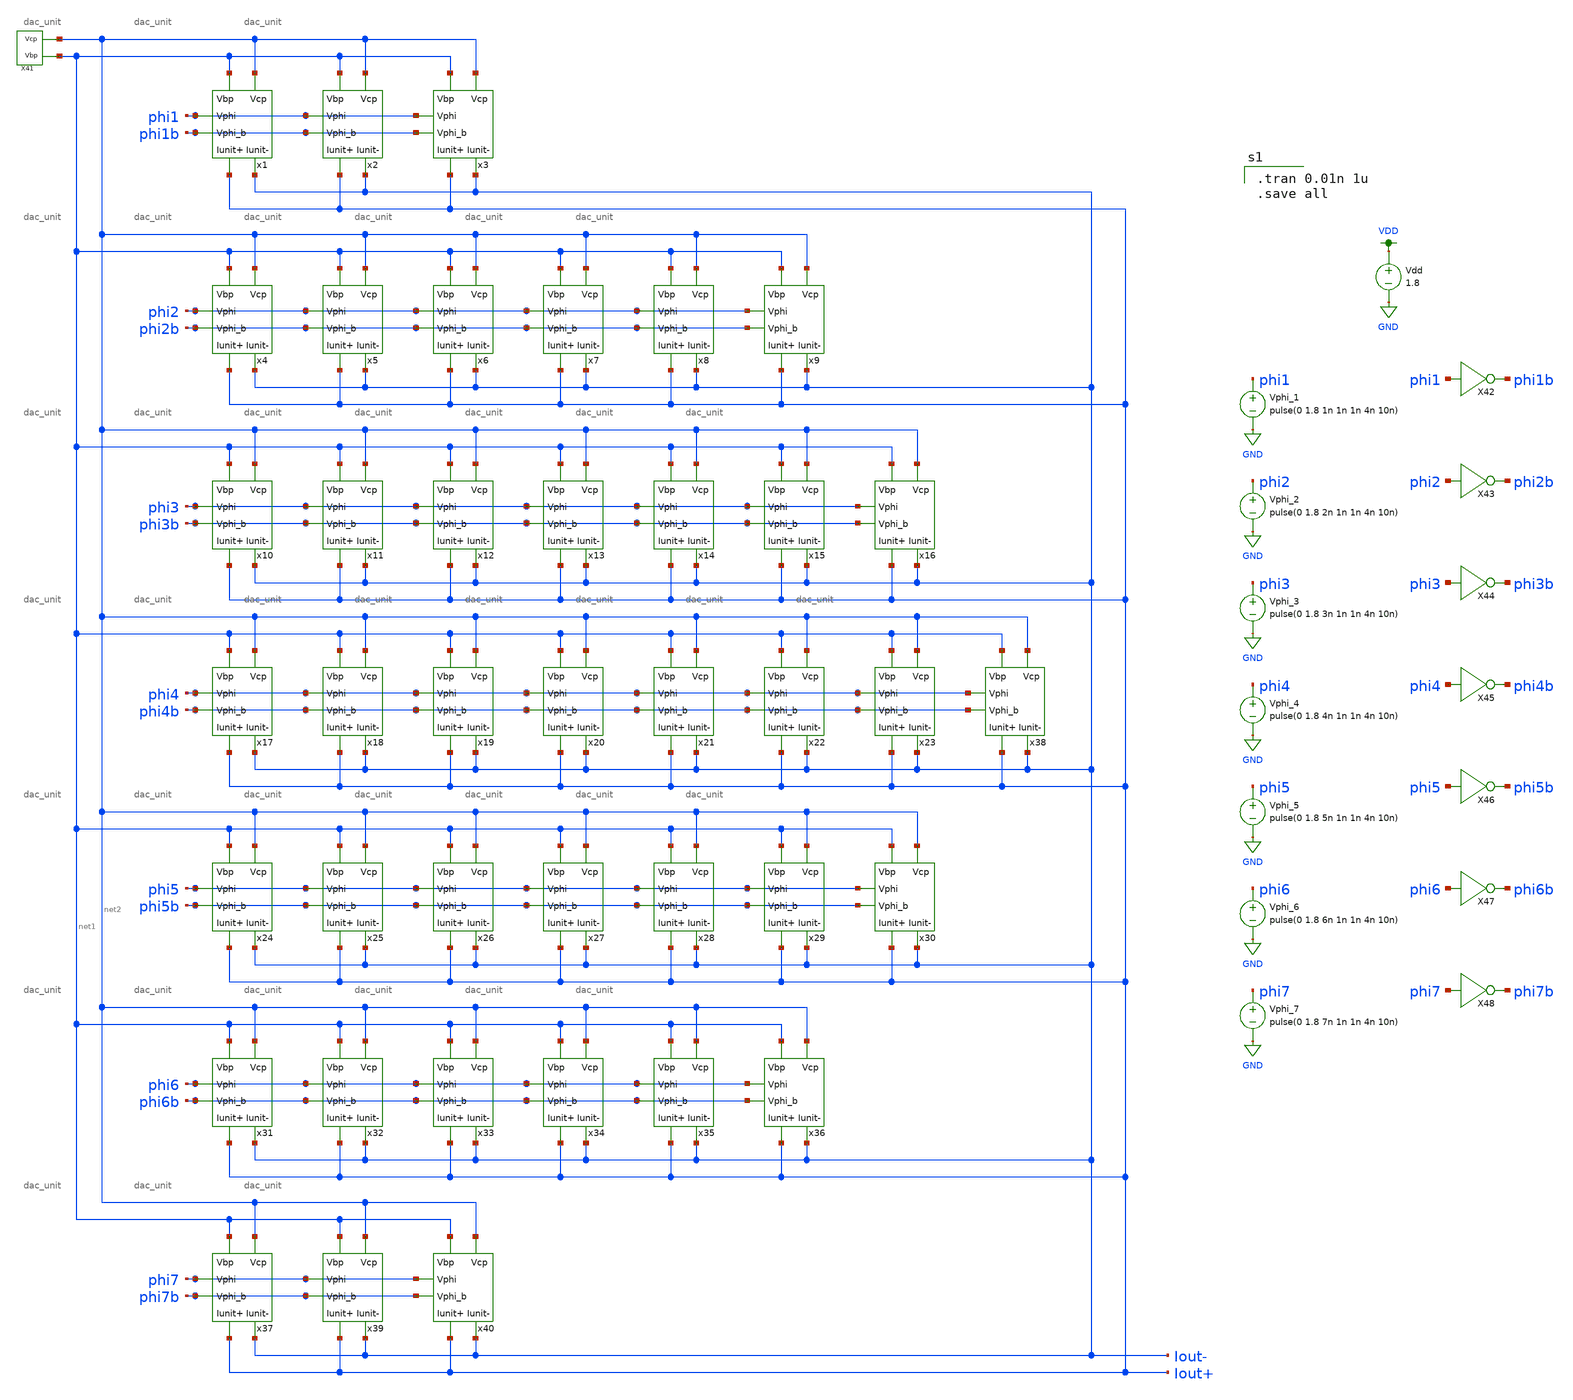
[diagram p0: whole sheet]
** sch_path: simulation/dac/dac.sch
**.subckt dac
x1 net1 net2 Iout+ Iout- phi1 phi1b dac_unit
x2 net1 net2 Iout+ Iout- phi1 phi1b dac_unit
x3 net1 net2 Iout+ Iout- phi1 phi1b dac_unit
x4 net1 net2 Iout+ Iout- phi2 phi2b dac_unit
x5 net1 net2 Iout+ Iout- phi2 phi2b dac_unit
x6 net1 net2 Iout+ Iout- phi2 phi2b dac_unit
x7 net1 net2 Iout+ Iout- phi2 phi2b dac_unit
x8 net1 net2 Iout+ Iout- phi2 phi2b dac_unit
x9 net1 net2 Iout+ Iout- phi2 phi2b dac_unit
x10 net1 net2 Iout+ Iout- phi3 phi3b dac_unit
x11 net1 net2 Iout+ Iout- phi3 phi3b dac_unit
x12 net1 net2 Iout+ Iout- phi3 phi3b dac_unit
x13 net1 net2 Iout+ Iout- phi3 phi3b dac_unit
x14 net1 net2 Iout+ Iout- phi3 phi3b dac_unit
x15 net1 net2 Iout+ Iout- phi3 phi3b dac_unit
x16 net1 net2 Iout+ Iout- phi3 phi3b dac_unit
x17 net1 net2 Iout+ Iout- phi4 phi4b dac_unit
x18 net1 net2 Iout+ Iout- phi4 phi4b dac_unit
x19 net1 net2 Iout+ Iout- phi4 phi4b dac_unit
x20 net1 net2 Iout+ Iout- phi4 phi4b dac_unit
x21 net1 net2 Iout+ Iout- phi4 phi4b dac_unit
x22 net1 net2 Iout+ Iout- phi4 phi4b dac_unit
x23 net1 net2 Iout+ Iout- phi4 phi4b dac_unit
x24 net1 net2 Iout+ Iout- phi5 phi5b dac_unit
x25 net1 net2 Iout+ Iout- phi5 phi5b dac_unit
x26 net1 net2 Iout+ Iout- phi5 phi5b dac_unit
x27 net1 net2 Iout+ Iout- phi5 phi5b dac_unit
x28 net1 net2 Iout+ Iout- phi5 phi5b dac_unit
x29 net1 net2 Iout+ Iout- phi5 phi5b dac_unit
x30 net1 net2 Iout+ Iout- phi5 phi5b dac_unit
x31 net1 net2 Iout+ Iout- phi6 phi6b dac_unit
x32 net1 net2 Iout+ Iout- phi6 phi6b dac_unit
x33 net1 net2 Iout+ Iout- phi6 phi6b dac_unit
x34 net1 net2 Iout+ Iout- phi6 phi6b dac_unit
x35 net1 net2 Iout+ Iout- phi6 phi6b dac_unit
x36 net1 net2 Iout+ Iout- phi6 phi6b dac_unit
x38 net1 net2 Iout+ Iout- phi4 phi4b dac_unit
x37 net1 net2 Iout+ Iout- phi7 phi7b dac_unit
x39 net1 net2 Iout+ Iout- phi7 phi7b dac_unit
x40 net1 net2 Iout+ Iout- phi7 phi7b dac_unit
X41 net2 net1 v_gen_lds
Vdd VDD GND 1.8
Vphi_1 phi1 GND pulse(0 1.8 1n 1n 1n 4n 10n)
Vphi_2 phi2 GND pulse(0 1.8 2n 1n 1n 4n 10n)
Vphi_3 phi3 GND pulse(0 1.8 3n 1n 1n 4n 10n)
Vphi_4 phi4 GND pulse(0 1.8 4n 1n 1n 4n 10n)
Vphi_5 phi5 GND pulse(0 1.8 5n 1n 1n 4n 10n)
Vphi_6 phi6 GND pulse(0 1.8 6n 1n 1n 4n 10n)
Vphi_7 phi7 GND pulse(0 1.8 7n 1n 1n 4n 10n)
X42 phi1 phi1b inverter
X43 phi2 phi2b inverter
X44 phi3 phi3b inverter
X45 phi4 phi4b inverter
X46 phi5 phi5b inverter
X47 phi6 phi6b inverter
X48 phi7 phi7b inverter
**** begin user architecture code

.option wnflag=1
.lib ~/skywater/skywater-pdk/libraries/sky130_fd_pr_ngspice/latest/models/sky130.lib.spice tt


.tran 0.01n 1u
.save all

**** end user architecture code
**.ends

* expanding   symbol:  ./dac_unit.sym # of pins=6
** sym_path: simulation/dac/dac_unit.sym
** sch_path: simulation/dac/dac_unit.sch
.subckt dac_unit Vbp Vcp Iunit+ Iunit- Vphi Vphi_b
*.ipin Vphi
*.ipin Vbp
*.ipin Vcp
*.opin Iunit-
*.opin Iunit+
*.ipin Vphi_b
XM1 net1 Vbp VDD VDD sky130_fd_pr__pfet_01v8 L=0.5 W=12 nf=1 ad='int((nf+1)/2) * W/nf * 0.29' as='int((nf+2)/2) * W/nf * 0.29'
+ pd='2*int((nf+1)/2) * (W/nf + 0.29)' ps='2*int((nf+2)/2) * (W/nf + 0.29)' nrd='0.29 / W' nrs='0.29 / W'
+ sa=0 sb=0 sd=0 mult=1 m=1
XM2 net2 Vcp net1 VDD sky130_fd_pr__pfet_01v8 L=0.5 W=12 nf=1 ad='int((nf+1)/2) * W/nf * 0.29' as='int((nf+2)/2) * W/nf * 0.29'
+ pd='2*int((nf+1)/2) * (W/nf + 0.29)' ps='2*int((nf+2)/2) * (W/nf + 0.29)' nrd='0.29 / W' nrs='0.29 / W'
+ sa=0 sb=0 sd=0 mult=1 m=1
XM3 Iunit- Vphi net2 VDD sky130_fd_pr__pfet_01v8 L=0.5 W=12 nf=1 ad='int((nf+1)/2) * W/nf * 0.29' as='int((nf+2)/2) * W/nf * 0.29'
+ pd='2*int((nf+1)/2) * (W/nf + 0.29)' ps='2*int((nf+2)/2) * (W/nf + 0.29)' nrd='0.29 / W' nrs='0.29 / W'
+ sa=0 sb=0 sd=0 mult=1 m=1
XM4 Iunit+ Vphi_b net2 VDD sky130_fd_pr__pfet_01v8 L=0.5 W=12 nf=1 ad='int((nf+1)/2) * W/nf * 0.29' as='int((nf+2)/2) * W/nf * 0.29'
+ pd='2*int((nf+1)/2) * (W/nf + 0.29)' ps='2*int((nf+2)/2) * (W/nf + 0.29)' nrd='0.29 / W' nrs='0.29 / W'
+ sa=0 sb=0 sd=0 mult=1 m=1
.ends


* expanding   symbol:  ./v_gen_lds.sym # of pins=2
** sym_path: simulation/dac/v_gen_lds.sym
** sch_path: simulation/dac/v_gen_lds.sch
.subckt v_gen_lds Vcp Vbp
*.opin Vcp
*.opin Vbp
XM25 net1 Vcp Vcp VDD sky130_fd_pr__pfet_01v8 L=0.5 W=12 nf=1 ad='int((nf+1)/2) * W/nf * 0.29' as='int((nf+2)/2) * W/nf * 0.29'
+ pd='2*int((nf+1)/2) * (W/nf + 0.29)' ps='2*int((nf+2)/2) * (W/nf + 0.29)' nrd='0.29 / W' nrs='0.29 / W'
+ sa=0 sb=0 sd=0 mult=1 m=1
XM26 Vcp net3 GND GND sky130_fd_pr__nfet_01v8 L=0.5 W=12 nf=1 ad='int((nf+1)/2) * W/nf * 0.29' as='int((nf+2)/2) * W/nf * 0.29'
+ pd='2*int((nf+1)/2) * (W/nf + 0.29)' ps='2*int((nf+2)/2) * (W/nf + 0.29)' nrd='0.29 / W' nrs='0.29 / W'
+ sa=0 sb=0 sd=0 mult=1 m=1
XM27 net2 net2 net1 VDD sky130_fd_pr__pfet_01v8 L=0.5 W=12 nf=1 ad='int((nf+1)/2) * W/nf * 0.29' as='int((nf+2)/2) * W/nf * 0.29'
+ pd='2*int((nf+1)/2) * (W/nf + 0.29)' ps='2*int((nf+2)/2) * (W/nf + 0.29)' nrd='0.29 / W' nrs='0.29 / W'
+ sa=0 sb=0 sd=0 mult=1 m=1
XM28 GND net3 net4 GND sky130_fd_pr__nfet_01v8 L=0.5 W=12 nf=1 ad='int((nf+1)/2) * W/nf * 0.29' as='int((nf+2)/2) * W/nf * 0.29'
+ pd='2*int((nf+1)/2) * (W/nf + 0.29)' ps='2*int((nf+2)/2) * (W/nf + 0.29)' nrd='0.29 / W' nrs='0.29 / W'
+ sa=0 sb=0 sd=0 mult=1 m=1
XM41 net1 net2 net2 VDD sky130_fd_pr__pfet_01v8 L=0.5 W=12 nf=1 ad='int((nf+1)/2) * W/nf * 0.29' as='int((nf+2)/2) * W/nf * 0.29'
+ pd='2*int((nf+1)/2) * (W/nf + 0.29)' ps='2*int((nf+2)/2) * (W/nf + 0.29)' nrd='0.29 / W' nrs='0.29 / W'
+ sa=0 sb=0 sd=0 mult=1 m=1
XM42 net4 net3 net5 GND sky130_fd_pr__nfet_01v8 L=0.5 W=12 nf=1 ad='int((nf+1)/2) * W/nf * 0.29' as='int((nf+2)/2) * W/nf * 0.29'
+ pd='2*int((nf+1)/2) * (W/nf + 0.29)' ps='2*int((nf+2)/2) * (W/nf + 0.29)' nrd='0.29 / W' nrs='0.29 / W'
+ sa=0 sb=0 sd=0 mult=1 m=1
XM43 net2 net2 net1 VDD sky130_fd_pr__pfet_01v8 L=0.5 W=12 nf=1 ad='int((nf+1)/2) * W/nf * 0.29' as='int((nf+2)/2) * W/nf * 0.29'
+ pd='2*int((nf+1)/2) * (W/nf + 0.29)' ps='2*int((nf+2)/2) * (W/nf + 0.29)' nrd='0.29 / W' nrs='0.29 / W'
+ sa=0 sb=0 sd=0 mult=1 m=1
XM44 net5 net3 net6 GND sky130_fd_pr__nfet_01v8 L=0.5 W=12 nf=1 ad='int((nf+1)/2) * W/nf * 0.29' as='int((nf+2)/2) * W/nf * 0.29'
+ pd='2*int((nf+1)/2) * (W/nf + 0.29)' ps='2*int((nf+2)/2) * (W/nf + 0.29)' nrd='0.29 / W' nrs='0.29 / W'
+ sa=0 sb=0 sd=0 mult=1 m=1
XM45 net1 net2 net2 VDD sky130_fd_pr__pfet_01v8 L=0.5 W=12 nf=1 ad='int((nf+1)/2) * W/nf * 0.29' as='int((nf+2)/2) * W/nf * 0.29'
+ pd='2*int((nf+1)/2) * (W/nf + 0.29)' ps='2*int((nf+2)/2) * (W/nf + 0.29)' nrd='0.29 / W' nrs='0.29 / W'
+ sa=0 sb=0 sd=0 mult=1 m=1
XM46 net6 net3 net7 GND sky130_fd_pr__nfet_01v8 L=0.5 W=12 nf=1 ad='int((nf+1)/2) * W/nf * 0.29' as='int((nf+2)/2) * W/nf * 0.29'
+ pd='2*int((nf+1)/2) * (W/nf + 0.29)' ps='2*int((nf+2)/2) * (W/nf + 0.29)' nrd='0.29 / W' nrs='0.29 / W'
+ sa=0 sb=0 sd=0 mult=1 m=1
XM47 VDD net2 net1 VDD sky130_fd_pr__pfet_01v8 L=0.5 W=12 nf=1 ad='int((nf+1)/2) * W/nf * 0.29' as='int((nf+2)/2) * W/nf * 0.29'
+ pd='2*int((nf+1)/2) * (W/nf + 0.29)' ps='2*int((nf+2)/2) * (W/nf + 0.29)' nrd='0.29 / W' nrs='0.29 / W'
+ sa=0 sb=0 sd=0 mult=1 m=1
XM48 net7 net3 net2 GND sky130_fd_pr__nfet_01v8 L=0.5 W=12 nf=1 ad='int((nf+1)/2) * W/nf * 0.29' as='int((nf+2)/2) * W/nf * 0.29'
+ pd='2*int((nf+1)/2) * (W/nf + 0.29)' ps='2*int((nf+2)/2) * (W/nf + 0.29)' nrd='0.29 / W' nrs='0.29 / W'
+ sa=0 sb=0 sd=0 mult=1 m=1
XM54 VDD Vbp Vbp VDD sky130_fd_pr__pfet_01v8 L=0.5 W=12 nf=1 ad='int((nf+1)/2) * W/nf * 0.29' as='int((nf+2)/2) * W/nf * 0.29'
+ pd='2*int((nf+1)/2) * (W/nf + 0.29)' ps='2*int((nf+2)/2) * (W/nf + 0.29)' nrd='0.29 / W' nrs='0.29 / W'
+ sa=0 sb=0 sd=0 mult=1 m=1
XM1 Vbp net3 GND GND sky130_fd_pr__nfet_01v8 L=0.5 W=12 nf=1 ad='int((nf+1)/2) * W/nf * 0.29' as='int((nf+2)/2) * W/nf * 0.29'
+ pd='2*int((nf+1)/2) * (W/nf + 0.29)' ps='2*int((nf+2)/2) * (W/nf + 0.29)' nrd='0.29 / W' nrs='0.29 / W'
+ sa=0 sb=0 sd=0 mult=1 m=1
XM2 net3 net3 GND GND sky130_fd_pr__nfet_01v8 L=0.5 W=12 nf=1 ad='int((nf+1)/2) * W/nf * 0.29' as='int((nf+2)/2) * W/nf * 0.29'
+ pd='2*int((nf+1)/2) * (W/nf + 0.29)' ps='2*int((nf+2)/2) * (W/nf + 0.29)' nrd='0.29 / W' nrs='0.29 / W'
+ sa=0 sb=0 sd=0 mult=1 m=1
XM3 Vcp VDD VDD VDD sky130_fd_pr__pfet_01v8 L=0.5 W=12 nf=1 ad='int((nf+1)/2) * W/nf * 0.29' as='int((nf+2)/2) * W/nf * 0.29'
+ pd='2*int((nf+1)/2) * (W/nf + 0.29)' ps='2*int((nf+2)/2) * (W/nf + 0.29)' nrd='0.29 / W' nrs='0.29 / W'
+ sa=0 sb=0 sd=0 mult=1 m=1
XM16 net8 net13 net13 VDD sky130_fd_pr__pfet_01v8 L=0.5 W=12 nf=1 ad='int((nf+1)/2) * W/nf * 0.29' as='int((nf+2)/2) * W/nf * 0.29'
+ pd='2*int((nf+1)/2) * (W/nf + 0.29)' ps='2*int((nf+2)/2) * (W/nf + 0.29)' nrd='0.29 / W' nrs='0.29 / W'
+ sa=0 sb=0 sd=0 mult=1 m=1
XM17 net13 net3 GND GND sky130_fd_pr__nfet_01v8 L=0.5 W=12 nf=1 ad='int((nf+1)/2) * W/nf * 0.29' as='int((nf+2)/2) * W/nf * 0.29'
+ pd='2*int((nf+1)/2) * (W/nf + 0.29)' ps='2*int((nf+2)/2) * (W/nf + 0.29)' nrd='0.29 / W' nrs='0.29 / W'
+ sa=0 sb=0 sd=0 mult=1 m=1
XM18 net2 net2 net8 VDD sky130_fd_pr__pfet_01v8 L=0.5 W=12 nf=1 ad='int((nf+1)/2) * W/nf * 0.29' as='int((nf+2)/2) * W/nf * 0.29'
+ pd='2*int((nf+1)/2) * (W/nf + 0.29)' ps='2*int((nf+2)/2) * (W/nf + 0.29)' nrd='0.29 / W' nrs='0.29 / W'
+ sa=0 sb=0 sd=0 mult=1 m=1
XM19 GND net3 net9 GND sky130_fd_pr__nfet_01v8 L=0.5 W=12 nf=1 ad='int((nf+1)/2) * W/nf * 0.29' as='int((nf+2)/2) * W/nf * 0.29'
+ pd='2*int((nf+1)/2) * (W/nf + 0.29)' ps='2*int((nf+2)/2) * (W/nf + 0.29)' nrd='0.29 / W' nrs='0.29 / W'
+ sa=0 sb=0 sd=0 mult=1 m=1
XM20 net8 net2 net2 VDD sky130_fd_pr__pfet_01v8 L=0.5 W=12 nf=1 ad='int((nf+1)/2) * W/nf * 0.29' as='int((nf+2)/2) * W/nf * 0.29'
+ pd='2*int((nf+1)/2) * (W/nf + 0.29)' ps='2*int((nf+2)/2) * (W/nf + 0.29)' nrd='0.29 / W' nrs='0.29 / W'
+ sa=0 sb=0 sd=0 mult=1 m=1
XM21 net9 net3 net10 GND sky130_fd_pr__nfet_01v8 L=0.5 W=12 nf=1 ad='int((nf+1)/2) * W/nf * 0.29' as='int((nf+2)/2) * W/nf * 0.29'
+ pd='2*int((nf+1)/2) * (W/nf + 0.29)' ps='2*int((nf+2)/2) * (W/nf + 0.29)' nrd='0.29 / W' nrs='0.29 / W'
+ sa=0 sb=0 sd=0 mult=1 m=1
XM22 net2 net2 net8 VDD sky130_fd_pr__pfet_01v8 L=0.5 W=12 nf=1 ad='int((nf+1)/2) * W/nf * 0.29' as='int((nf+2)/2) * W/nf * 0.29'
+ pd='2*int((nf+1)/2) * (W/nf + 0.29)' ps='2*int((nf+2)/2) * (W/nf + 0.29)' nrd='0.29 / W' nrs='0.29 / W'
+ sa=0 sb=0 sd=0 mult=1 m=1
XM23 net10 net3 net11 GND sky130_fd_pr__nfet_01v8 L=0.5 W=12 nf=1 ad='int((nf+1)/2) * W/nf * 0.29' as='int((nf+2)/2) * W/nf * 0.29'
+ pd='2*int((nf+1)/2) * (W/nf + 0.29)' ps='2*int((nf+2)/2) * (W/nf + 0.29)' nrd='0.29 / W' nrs='0.29 / W'
+ sa=0 sb=0 sd=0 mult=1 m=1
XM24 net8 net2 net2 VDD sky130_fd_pr__pfet_01v8 L=0.5 W=12 nf=1 ad='int((nf+1)/2) * W/nf * 0.29' as='int((nf+2)/2) * W/nf * 0.29'
+ pd='2*int((nf+1)/2) * (W/nf + 0.29)' ps='2*int((nf+2)/2) * (W/nf + 0.29)' nrd='0.29 / W' nrs='0.29 / W'
+ sa=0 sb=0 sd=0 mult=1 m=1
XM49 net11 net3 net12 GND sky130_fd_pr__nfet_01v8 L=0.5 W=12 nf=1 ad='int((nf+1)/2) * W/nf * 0.29' as='int((nf+2)/2) * W/nf * 0.29'
+ pd='2*int((nf+1)/2) * (W/nf + 0.29)' ps='2*int((nf+2)/2) * (W/nf + 0.29)' nrd='0.29 / W' nrs='0.29 / W'
+ sa=0 sb=0 sd=0 mult=1 m=1
XM50 VDD net2 net8 VDD sky130_fd_pr__pfet_01v8 L=0.5 W=12 nf=1 ad='int((nf+1)/2) * W/nf * 0.29' as='int((nf+2)/2) * W/nf * 0.29'
+ pd='2*int((nf+1)/2) * (W/nf + 0.29)' ps='2*int((nf+2)/2) * (W/nf + 0.29)' nrd='0.29 / W' nrs='0.29 / W'
+ sa=0 sb=0 sd=0 mult=1 m=1
XM51 net12 net3 net2 GND sky130_fd_pr__nfet_01v8 L=0.5 W=12 nf=1 ad='int((nf+1)/2) * W/nf * 0.29' as='int((nf+2)/2) * W/nf * 0.29'
+ pd='2*int((nf+1)/2) * (W/nf + 0.29)' ps='2*int((nf+2)/2) * (W/nf + 0.29)' nrd='0.29 / W' nrs='0.29 / W'
+ sa=0 sb=0 sd=0 mult=1 m=1
XM52 VDD Vbp Vbp VDD sky130_fd_pr__pfet_01v8 L=0.5 W=12 nf=1 ad='int((nf+1)/2) * W/nf * 0.29' as='int((nf+2)/2) * W/nf * 0.29'
+ pd='2*int((nf+1)/2) * (W/nf + 0.29)' ps='2*int((nf+2)/2) * (W/nf + 0.29)' nrd='0.29 / W' nrs='0.29 / W'
+ sa=0 sb=0 sd=0 mult=1 m=1
XM53 GND net3 Vbp GND sky130_fd_pr__nfet_01v8 L=0.5 W=12 nf=1 ad='int((nf+1)/2) * W/nf * 0.29' as='int((nf+2)/2) * W/nf * 0.29'
+ pd='2*int((nf+1)/2) * (W/nf + 0.29)' ps='2*int((nf+2)/2) * (W/nf + 0.29)' nrd='0.29 / W' nrs='0.29 / W'
+ sa=0 sb=0 sd=0 mult=1 m=1
XM55 net3 net3 GND GND sky130_fd_pr__nfet_01v8 L=0.5 W=12 nf=1 ad='int((nf+1)/2) * W/nf * 0.29' as='int((nf+2)/2) * W/nf * 0.29'
+ pd='2*int((nf+1)/2) * (W/nf + 0.29)' ps='2*int((nf+2)/2) * (W/nf + 0.29)' nrd='0.29 / W' nrs='0.29 / W'
+ sa=0 sb=0 sd=0 mult=1 m=1
XM56 net13 VDD VDD VDD sky130_fd_pr__pfet_01v8 L=0.5 W=12 nf=1 ad='int((nf+1)/2) * W/nf * 0.29' as='int((nf+2)/2) * W/nf * 0.29'
+ pd='2*int((nf+1)/2) * (W/nf + 0.29)' ps='2*int((nf+2)/2) * (W/nf + 0.29)' nrd='0.29 / W' nrs='0.29 / W'
+ sa=0 sb=0 sd=0 mult=1 m=1
Ib GND net3 2u
.ends


* expanding   symbol:  ./inverter.sym # of pins=2
** sym_path: simulation/dac/inverter.sym
** sch_path: simulation/dac/inverter.sch
.subckt inverter A Y
*.ipin A
*.opin Y
XM1 Y A VDD VDD sky130_fd_pr__pfet_01v8 L=0.15 W=1 nf=1 ad='int((nf+1)/2) * W/nf * 0.29' as='int((nf+2)/2) * W/nf * 0.29'
+ pd='2*int((nf+1)/2) * (W/nf + 0.29)' ps='2*int((nf+2)/2) * (W/nf + 0.29)' nrd='0.29 / W' nrs='0.29 / W'
+ sa=0 sb=0 sd=0 mult=1 m=1
XM2 Y A GND GND sky130_fd_pr__nfet_01v8 L=0.15 W=1 nf=1 ad='int((nf+1)/2) * W/nf * 0.29' as='int((nf+2)/2) * W/nf * 0.29'
+ pd='2*int((nf+1)/2) * (W/nf + 0.29)' ps='2*int((nf+2)/2) * (W/nf + 0.29)' nrd='0.29 / W' nrs='0.29 / W'
+ sa=0 sb=0 sd=0 mult=1 m=1
.ends

.GLOBAL VDD
.GLOBAL GND
.end
